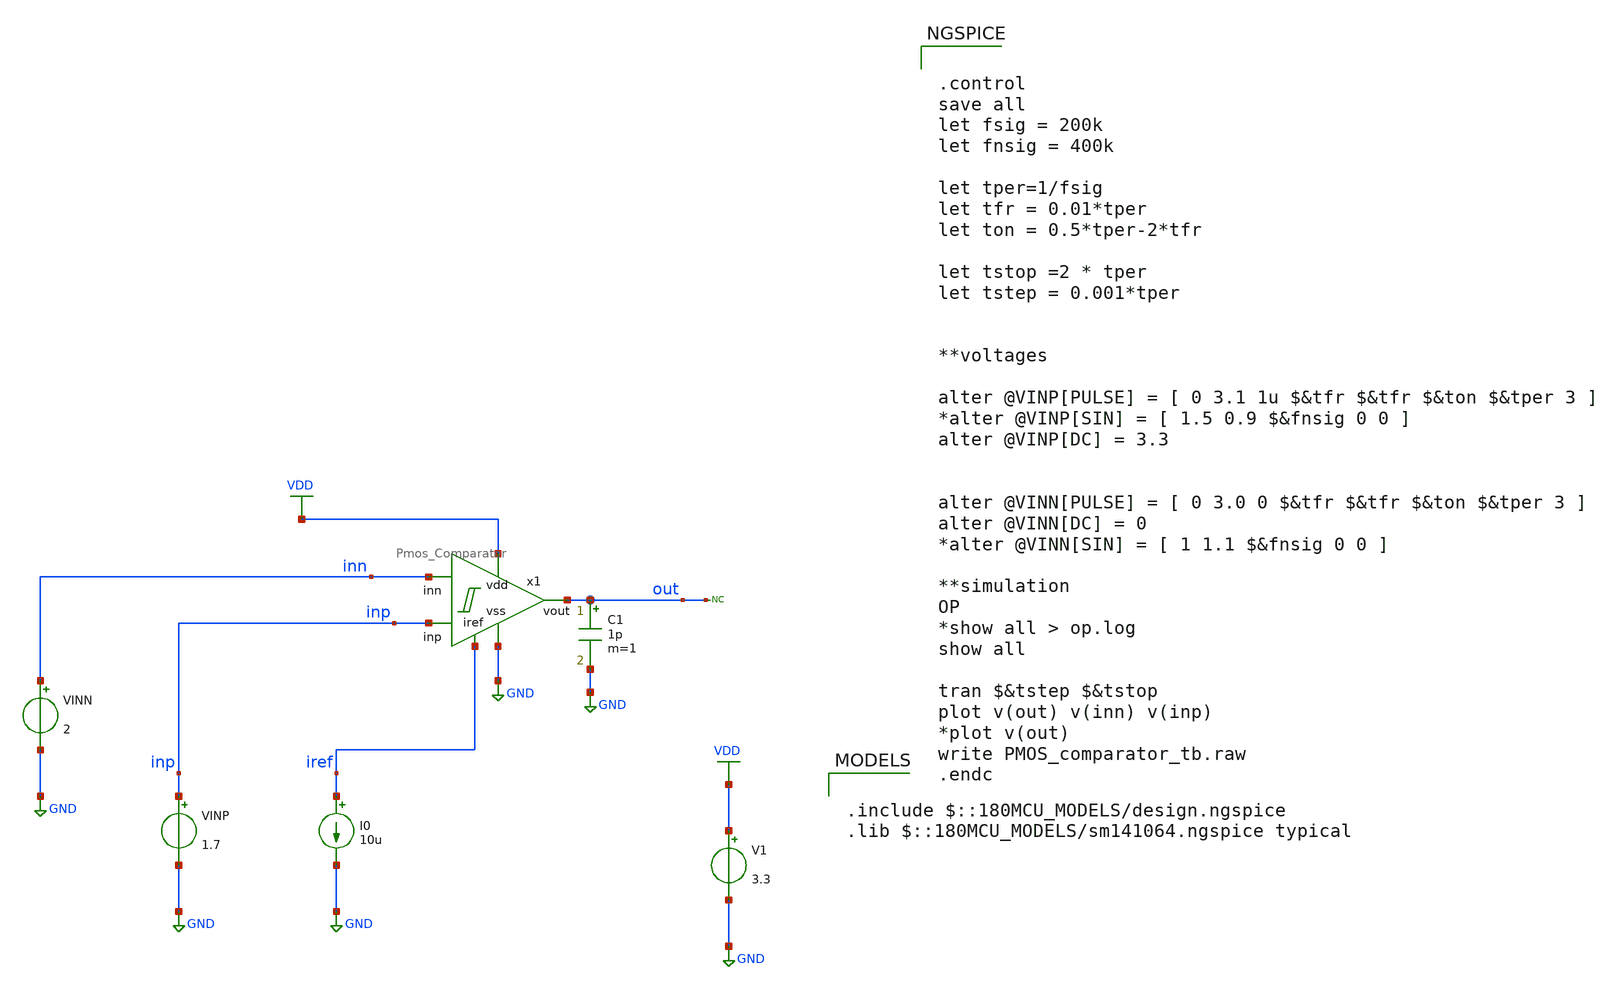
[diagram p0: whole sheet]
** sch_path: designs/libs/tb_analog/Comparator/PMOS_comparator_op_tb.sch
**.subckt PMOS_comparator_op_tb
I0 iref GND 10u
V1 VDD GND 3.3
VINP inp GND 1.7
C1 out GND 1p m=1
* noconn out
VINN inn GND 2
x1 VDD out inp GND inn iref Pmos_Comparator
**** begin user architecture code


.control
save all
let fsig = 200k
let fnsig = 400k

let tper=1/fsig
let tfr = 0.01*tper
let ton = 0.5*tper-2*tfr

let tstop =2 * tper
let tstep = 0.001*tper


**voltages

alter @VINP[PULSE] = [ 0 3.1 1u $&tfr $&tfr $&ton $&tper 3 ]
*alter @VINP[SIN] = [ 1.5 0.9 $&fnsig 0 0 ]
alter @VINP[DC] = 3.3


alter @VINN[PULSE] = [ 0 3.0 0 $&tfr $&tfr $&ton $&tper 3 ]
alter @VINN[DC] = 0
*alter @VINN[SIN] = [ 1 1.1 $&fnsig 0 0 ]

**simulation
OP
*show all > op.log
show all

tran $&tstep $&tstop
plot v(out) v(inn) v(inp)
*plot v(out)
write PMOS_comparator_tb.raw
.endc



.include $::180MCU_MODELS/design.ngspice
.lib $::180MCU_MODELS/sm141064.ngspice typical

**** end user architecture code
**.ends
.GLOBAL GND
.GLOBAL VDD
.end
